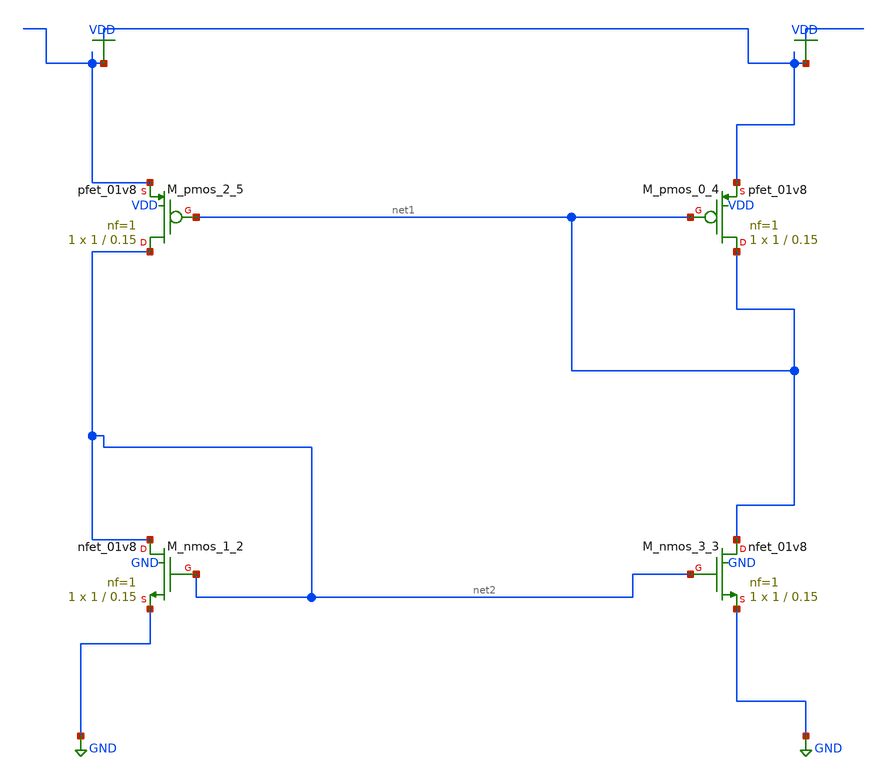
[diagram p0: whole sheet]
** sch_path: schematics/AMSNet/761.sch
**.subckt 761
XM_nmos_1_2 net2 net2 GND GND sky130_fd_pr__nfet_01v8 L=0.15 W=1 nf=1 ad='int((1 + 1)/2) * 1 / 1 * 0.29'
+ as='int((1 + 2)/2) * 1 / 1 * 0.29' pd='2*int((1 + 1)/2) * (1 / 1 + 0.29)' ps='2*int((1 + 2)/2) * (1 / 1 + 0.29)'
+ nrd='0.29 / 1 ' nrs='0.29 / 1 ' sa=0 sb=0 sd=0 mult=1 m=1
XM_nmos_3_3 net1 net2 GND GND sky130_fd_pr__nfet_01v8 L=0.15 W=1 nf=1 ad='int((1 + 1)/2) * 1 / 1 * 0.29'
+ as='int((1 + 2)/2) * 1 / 1 * 0.29' pd='2*int((1 + 1)/2) * (1 / 1 + 0.29)' ps='2*int((1 + 2)/2) * (1 / 1 + 0.29)'
+ nrd='0.29 / 1 ' nrs='0.29 / 1 ' sa=0 sb=0 sd=0 mult=1 m=1
XM_pmos_0_4 net1 net1 VDD VDD sky130_fd_pr__pfet_01v8 L=0.15 W=1 nf=1 ad='int((1 + 1)/2) * 1 / 1 * 0.29'
+ as='int((1 + 2)/2) * 1 / 1 * 0.29' pd='2*int((1 + 1)/2) * (1 / 1 + 0.29)' ps='2*int((1 + 2)/2) * (1 / 1 + 0.29)'
+ nrd='0.29 / 1 ' nrs='0.29 / 1 ' sa=0 sb=0 sd=0 mult=1 m=1
XM_pmos_2_5 net2 net1 VDD VDD sky130_fd_pr__pfet_01v8 L=0.15 W=1 nf=1 ad='int((1 + 1)/2) * 1 / 1 * 0.29'
+ as='int((1 + 2)/2) * 1 / 1 * 0.29' pd='2*int((1 + 1)/2) * (1 / 1 + 0.29)' ps='2*int((1 + 2)/2) * (1 / 1 + 0.29)'
+ nrd='0.29 / 1 ' nrs='0.29 / 1 ' sa=0 sb=0 sd=0 mult=1 m=1
**.ends
.GLOBAL GND
.GLOBAL VDD
.end
